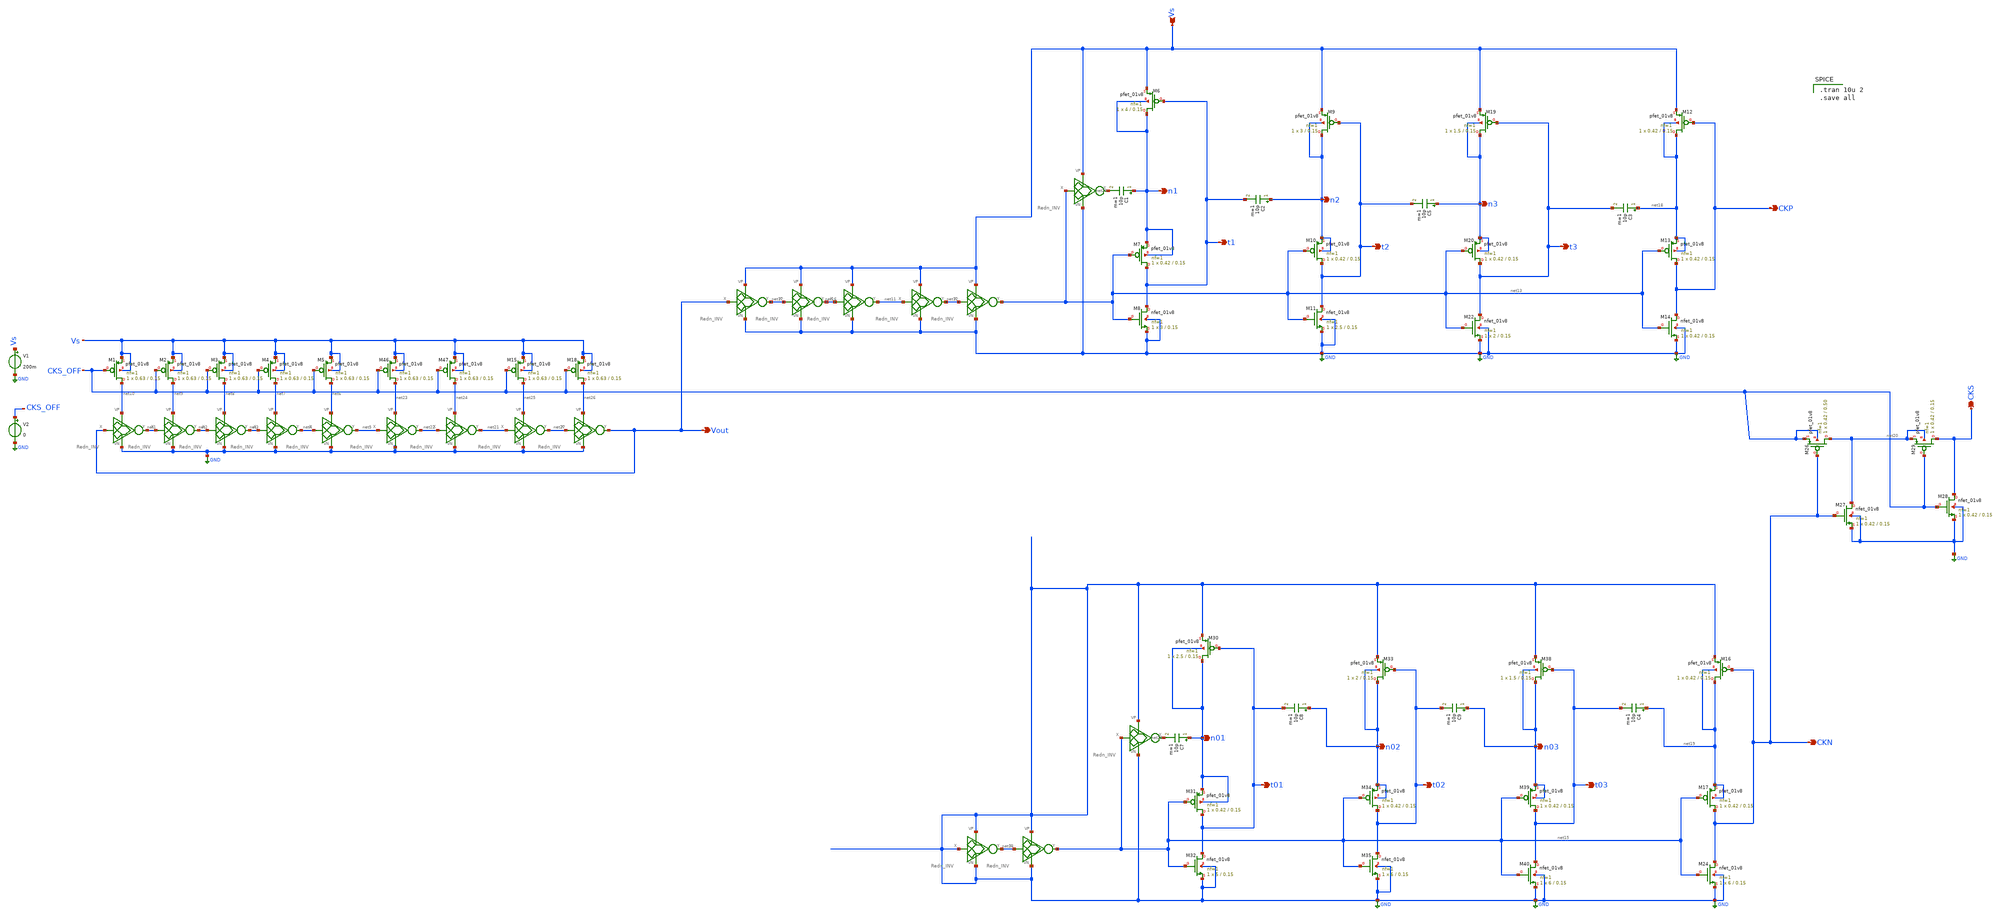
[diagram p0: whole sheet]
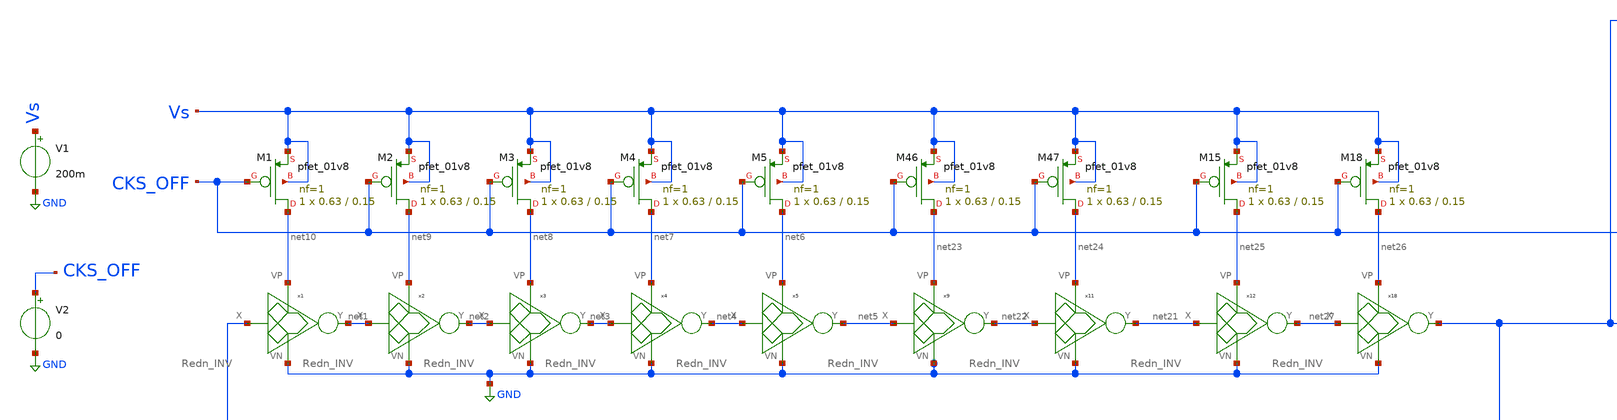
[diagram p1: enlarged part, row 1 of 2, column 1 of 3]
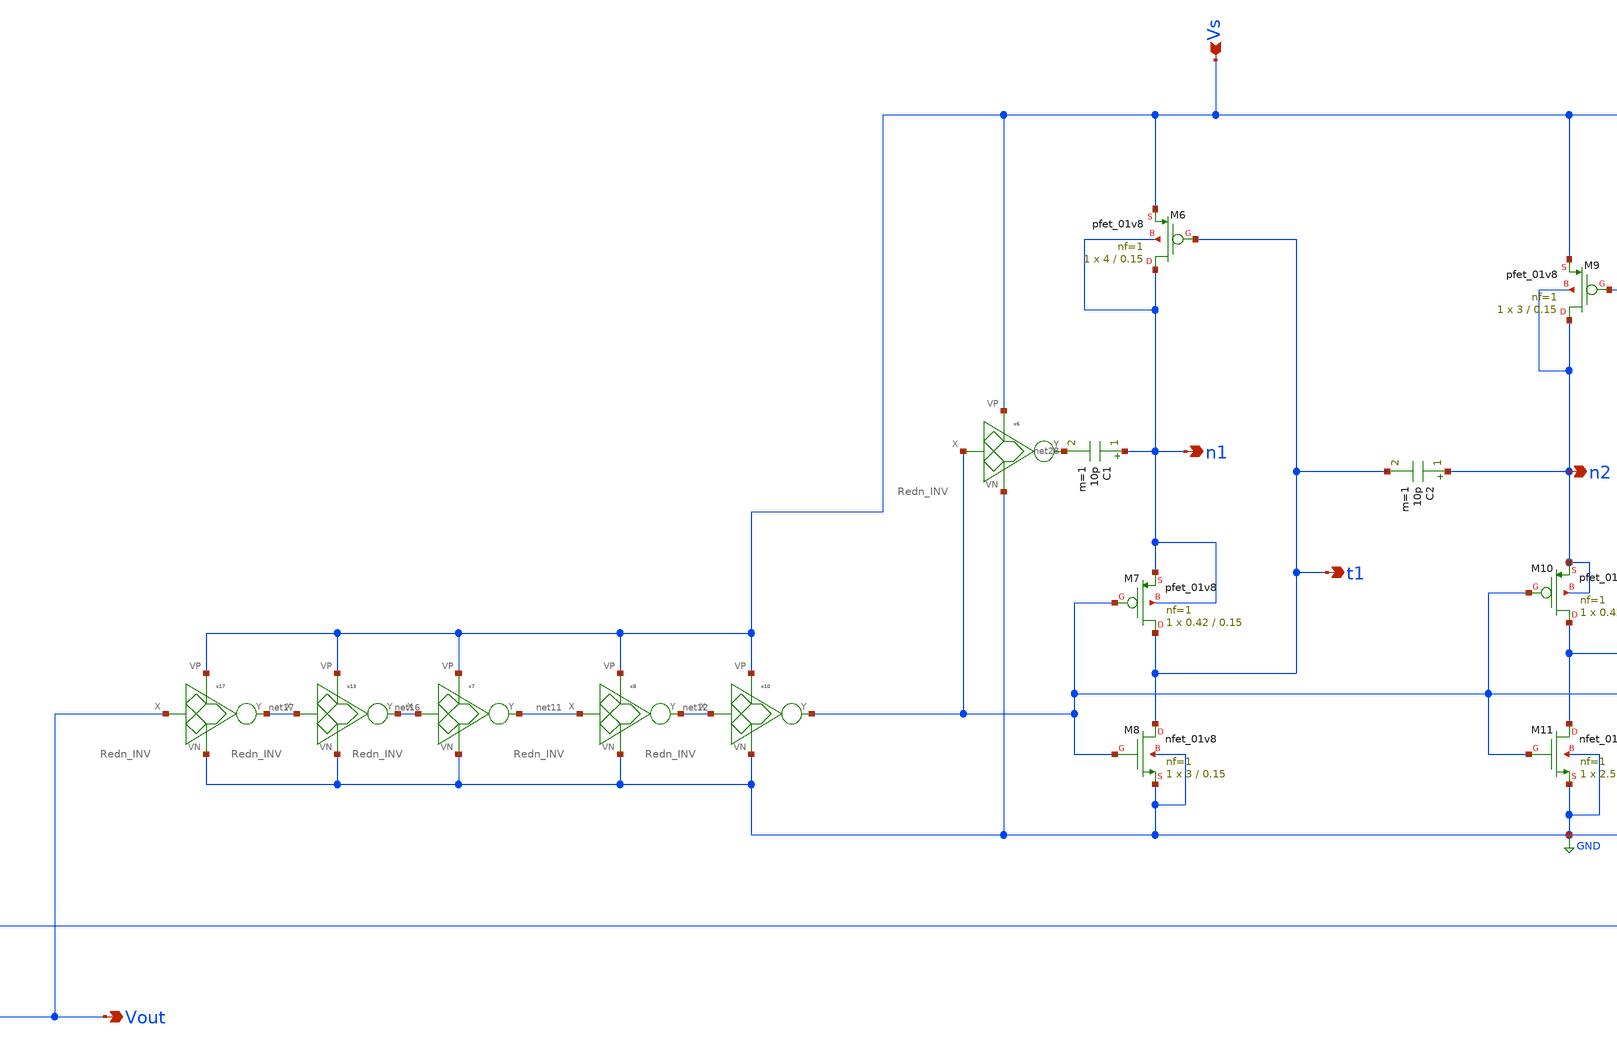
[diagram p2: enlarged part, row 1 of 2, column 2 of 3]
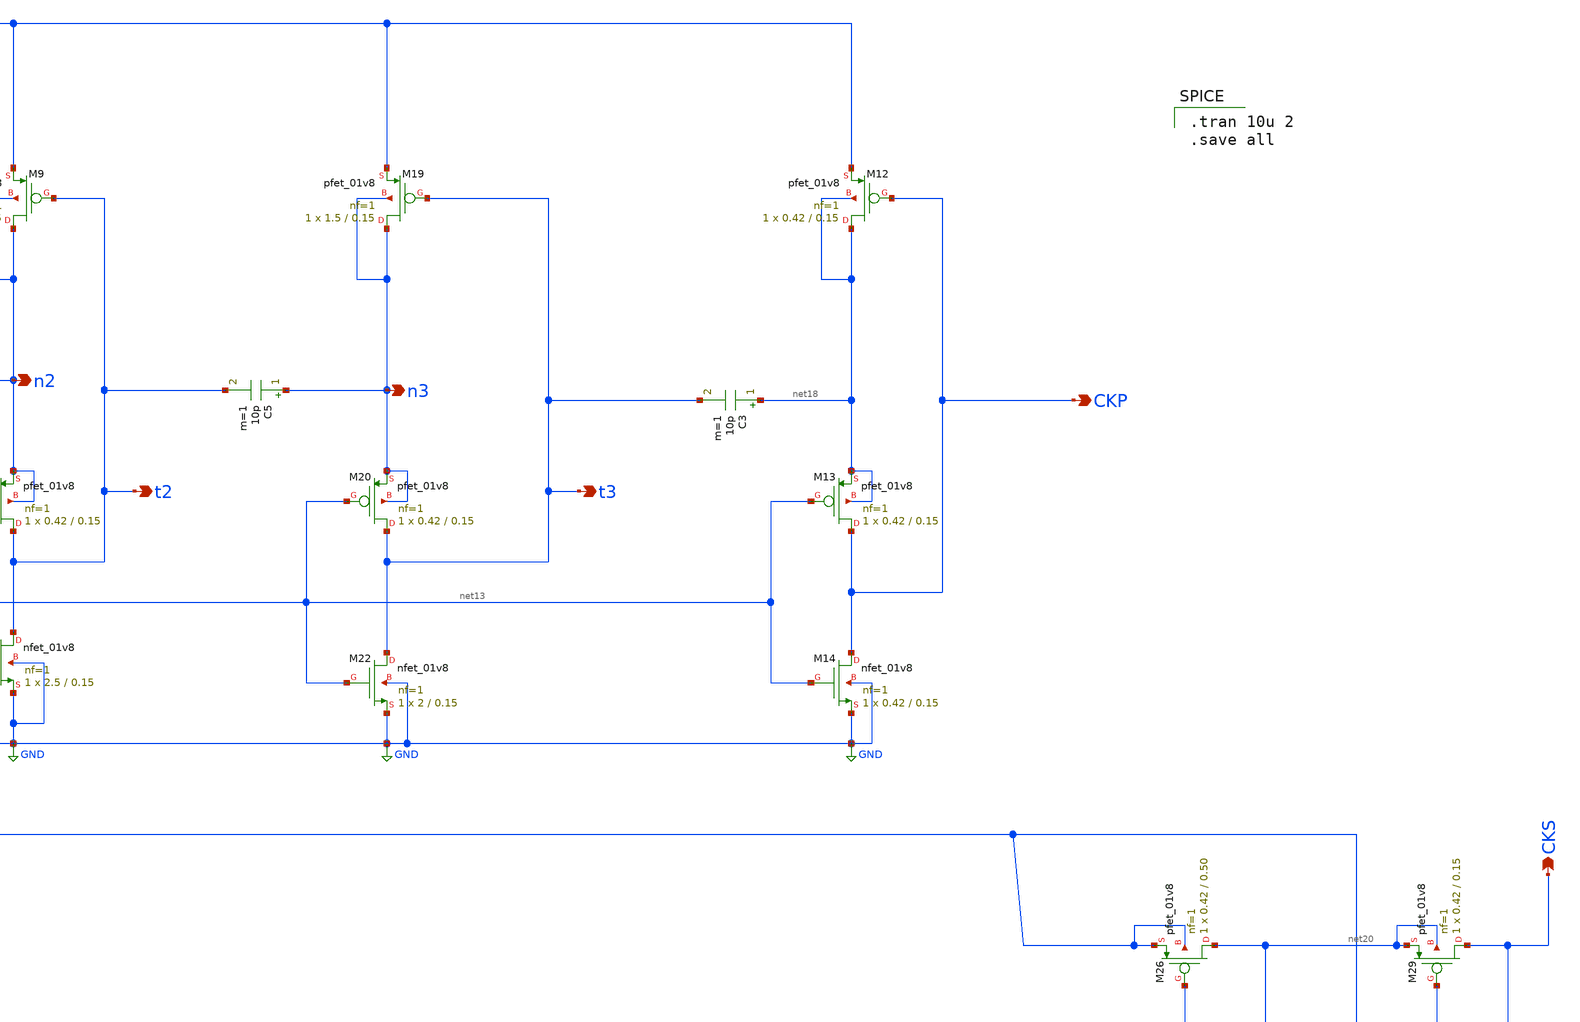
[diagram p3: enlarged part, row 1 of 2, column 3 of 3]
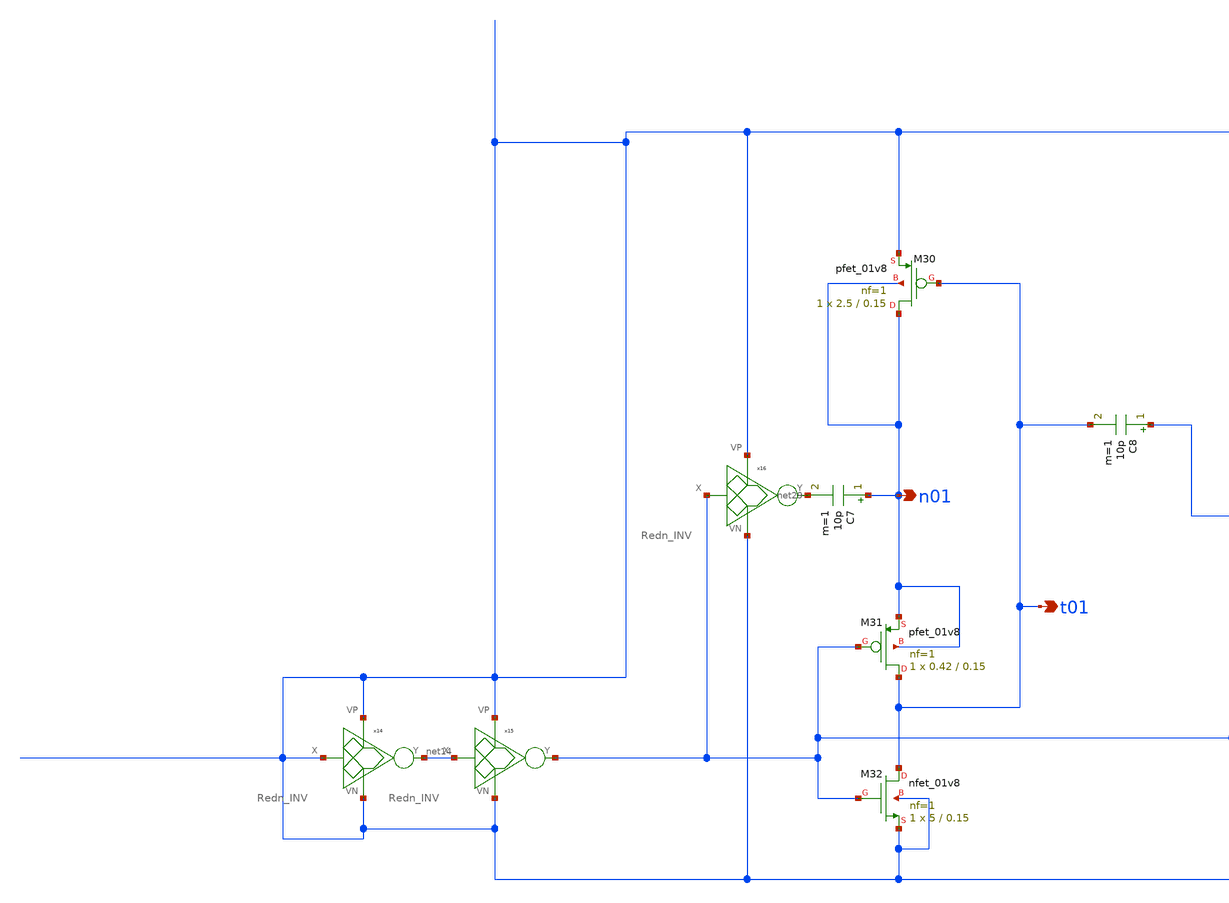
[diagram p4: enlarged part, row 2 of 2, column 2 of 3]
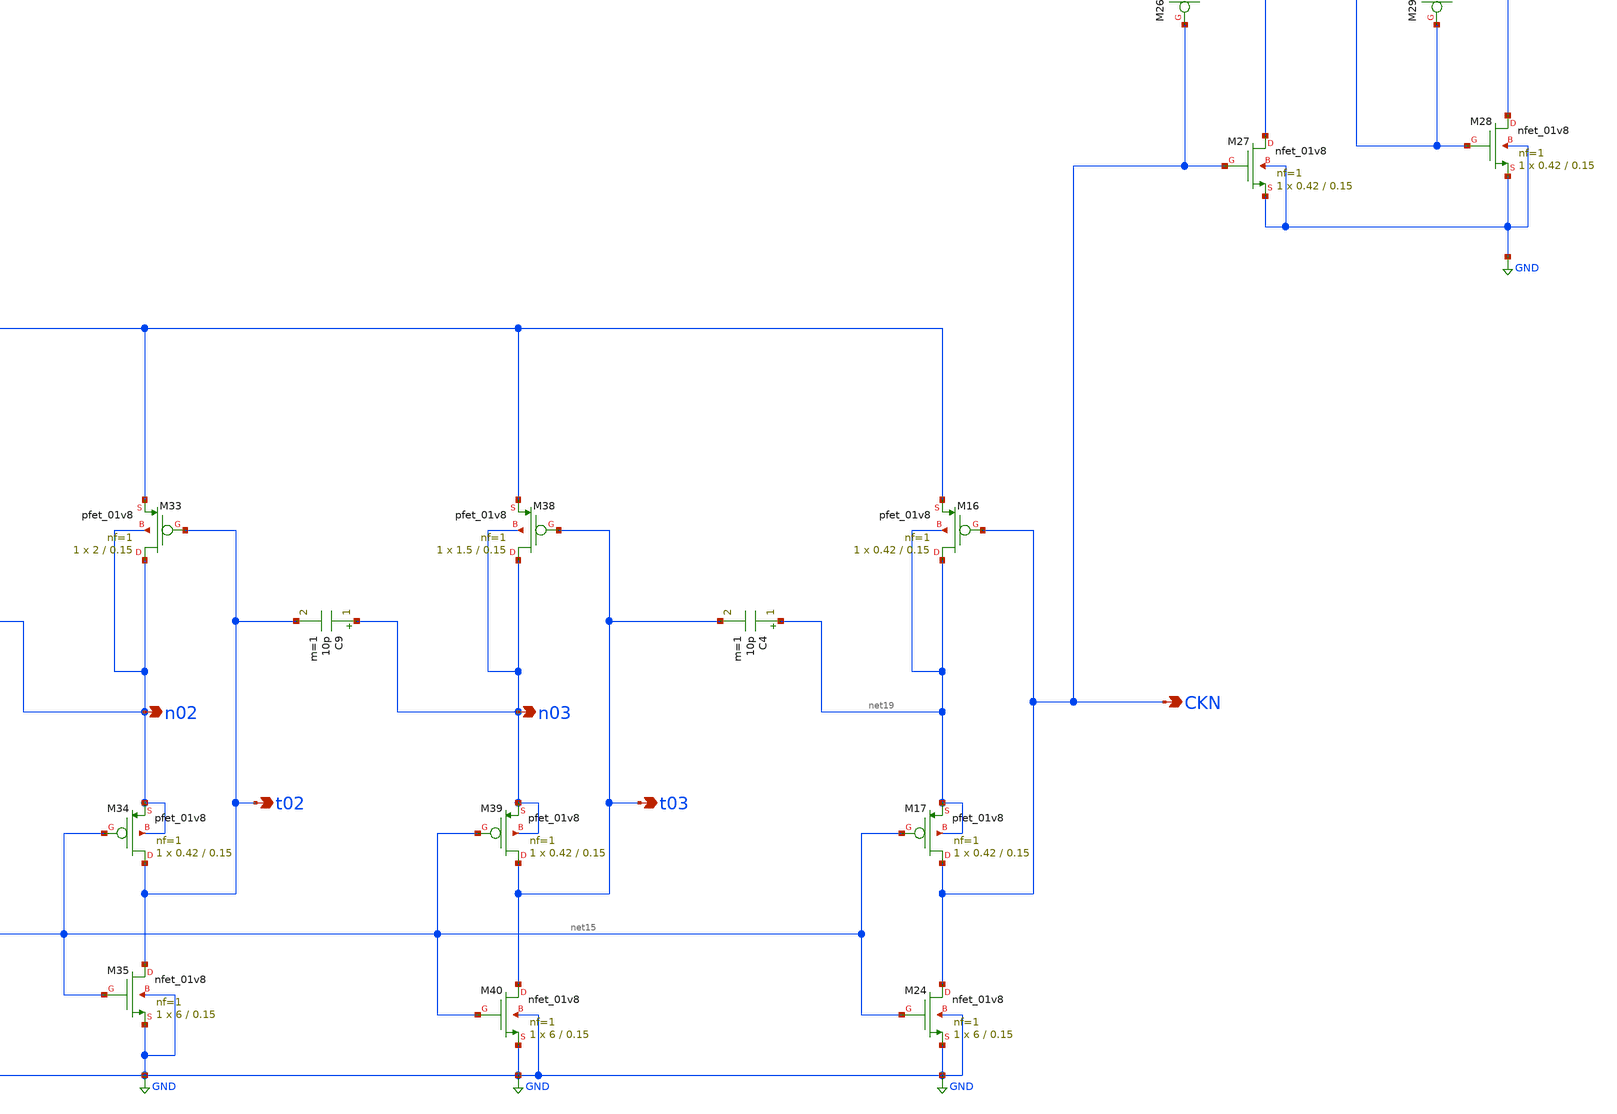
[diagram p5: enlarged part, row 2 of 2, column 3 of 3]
** sch_path: Blocks/Startup Converter/Startup_Conv_4.sch
**.subckt Startup_Conv_4 Vout Vs n1 t2 CKP CKN CKS t3 t1 n2 n3 t01 t02 t03 n01 n02 n03
*.opin Vout
*.ipin Vs
*.opin n1
*.opin t2
*.opin CKP
*.opin CKN
*.opin CKS
*.opin t3
*.opin t1
*.opin n2
*.opin n3
*.opin t01
*.opin t02
*.opin t03
*.opin n01
*.opin n02
*.opin n03
V1 Vs GND 200m
XM1 net10 CKS_OFF Vs Vs sky130_fd_pr__pfet_01v8 L=0.15 W=0.63 nf=1 ad='int((nf+1)/2) * W/nf * 0.29' as='int((nf+2)/2) * W/nf * 0.29'
+ pd='2*int((nf+1)/2) * (W/nf + 0.29)' ps='2*int((nf+2)/2) * (W/nf + 0.29)' nrd='0.29 / W' nrs='0.29 / W'
+ sa=0 sb=0 sd=0 mult=1 m=1
XM2 net9 CKS_OFF Vs Vs sky130_fd_pr__pfet_01v8 L=0.15 W=0.63 nf=1 ad='int((nf+1)/2) * W/nf * 0.29' as='int((nf+2)/2) * W/nf * 0.29'
+ pd='2*int((nf+1)/2) * (W/nf + 0.29)' ps='2*int((nf+2)/2) * (W/nf + 0.29)' nrd='0.29 / W' nrs='0.29 / W'
+ sa=0 sb=0 sd=0 mult=1 m=1
XM3 net8 CKS_OFF Vs Vs sky130_fd_pr__pfet_01v8 L=0.15 W=0.63 nf=1 ad='int((nf+1)/2) * W/nf * 0.29' as='int((nf+2)/2) * W/nf * 0.29'
+ pd='2*int((nf+1)/2) * (W/nf + 0.29)' ps='2*int((nf+2)/2) * (W/nf + 0.29)' nrd='0.29 / W' nrs='0.29 / W'
+ sa=0 sb=0 sd=0 mult=1 m=1
XM4 net7 CKS_OFF Vs Vs sky130_fd_pr__pfet_01v8 L=0.15 W=0.63 nf=1 ad='int((nf+1)/2) * W/nf * 0.29' as='int((nf+2)/2) * W/nf * 0.29'
+ pd='2*int((nf+1)/2) * (W/nf + 0.29)' ps='2*int((nf+2)/2) * (W/nf + 0.29)' nrd='0.29 / W' nrs='0.29 / W'
+ sa=0 sb=0 sd=0 mult=1 m=1
XM5 net6 CKS_OFF Vs Vs sky130_fd_pr__pfet_01v8 L=0.15 W=0.63 nf=1 ad='int((nf+1)/2) * W/nf * 0.29' as='int((nf+2)/2) * W/nf * 0.29'
+ pd='2*int((nf+1)/2) * (W/nf + 0.29)' ps='2*int((nf+2)/2) * (W/nf + 0.29)' nrd='0.29 / W' nrs='0.29 / W'
+ sa=0 sb=0 sd=0 mult=1 m=1
V2 CKS_OFF GND 0
x1 Vout net1 net10 GND Redn_INV
x2 net1 net2 net9 GND Redn_INV
x3 net2 net3 net8 GND Redn_INV
x4 net3 net4 net7 GND Redn_INV
x5 net4 net5 net6 GND Redn_INV
C1 n1 net28 10p m=1
XM6 n1 t1 Vs n1 sky130_fd_pr__pfet_01v8 L=0.15 W=4 nf=1 ad='int((nf+1)/2) * W/nf * 0.29' as='int((nf+2)/2) * W/nf * 0.29'
+ pd='2*int((nf+1)/2) * (W/nf + 0.29)' ps='2*int((nf+2)/2) * (W/nf + 0.29)' nrd='0.29 / W' nrs='0.29 / W'
+ sa=0 sb=0 sd=0 mult=1 m=1
XM7 t1 net13 n1 n1 sky130_fd_pr__pfet_01v8 L=0.15 W=0.42 nf=1 ad='int((nf+1)/2) * W/nf * 0.29' as='int((nf+2)/2) * W/nf * 0.29'
+ pd='2*int((nf+1)/2) * (W/nf + 0.29)' ps='2*int((nf+2)/2) * (W/nf + 0.29)' nrd='0.29 / W' nrs='0.29 / W'
+ sa=0 sb=0 sd=0 mult=1 m=1
XM8 t1 net13 GND GND sky130_fd_pr__nfet_01v8 L=0.15 W=3 nf=1 ad='int((nf+1)/2) * W/nf * 0.29' as='int((nf+2)/2) * W/nf * 0.29'
+ pd='2*int((nf+1)/2) * (W/nf + 0.29)' ps='2*int((nf+2)/2) * (W/nf + 0.29)' nrd='0.29 / W' nrs='0.29 / W'
+ sa=0 sb=0 sd=0 mult=1 m=1
XM9 n2 t2 Vs n2 sky130_fd_pr__pfet_01v8 L=0.15 W=3 nf=1 ad='int((nf+1)/2) * W/nf * 0.29' as='int((nf+2)/2) * W/nf * 0.29'
+ pd='2*int((nf+1)/2) * (W/nf + 0.29)' ps='2*int((nf+2)/2) * (W/nf + 0.29)' nrd='0.29 / W' nrs='0.29 / W'
+ sa=0 sb=0 sd=0 mult=1 m=1
XM10 t2 net13 n2 n2 sky130_fd_pr__pfet_01v8 L=0.15 W=0.42 nf=1 ad='int((nf+1)/2) * W/nf * 0.29' as='int((nf+2)/2) * W/nf * 0.29'
+ pd='2*int((nf+1)/2) * (W/nf + 0.29)' ps='2*int((nf+2)/2) * (W/nf + 0.29)' nrd='0.29 / W' nrs='0.29 / W'
+ sa=0 sb=0 sd=0 mult=1 m=1
XM11 t2 net13 GND GND sky130_fd_pr__nfet_01v8 L=0.15 W=2.5 nf=1 ad='int((nf+1)/2) * W/nf * 0.29' as='int((nf+2)/2) * W/nf * 0.29'
+ pd='2*int((nf+1)/2) * (W/nf + 0.29)' ps='2*int((nf+2)/2) * (W/nf + 0.29)' nrd='0.29 / W' nrs='0.29 / W'
+ sa=0 sb=0 sd=0 mult=1 m=1
C2 n2 t1 10p m=1
x7 net16 net11 Vs GND Redn_INV
x8 net11 net12 Vs GND Redn_INV
x10 net12 net13 Vs GND Redn_INV
x6 net13 net28 Vs GND Redn_INV
XM19 n3 t3 Vs n3 sky130_fd_pr__pfet_01v8 L=0.15 W=1.5 nf=1 ad='int((nf+1)/2) * W/nf * 0.29' as='int((nf+2)/2) * W/nf * 0.29'
+ pd='2*int((nf+1)/2) * (W/nf + 0.29)' ps='2*int((nf+2)/2) * (W/nf + 0.29)' nrd='0.29 / W' nrs='0.29 / W'
+ sa=0 sb=0 sd=0 mult=1 m=1
XM20 t3 net13 n3 n3 sky130_fd_pr__pfet_01v8 L=0.15 W=0.42 nf=1 ad='int((nf+1)/2) * W/nf * 0.29' as='int((nf+2)/2) * W/nf * 0.29'
+ pd='2*int((nf+1)/2) * (W/nf + 0.29)' ps='2*int((nf+2)/2) * (W/nf + 0.29)' nrd='0.29 / W' nrs='0.29 / W'
+ sa=0 sb=0 sd=0 mult=1 m=1
XM22 t3 net13 GND GND sky130_fd_pr__nfet_01v8 L=0.15 W=2 nf=1 ad='int((nf+1)/2) * W/nf * 0.29' as='int((nf+2)/2) * W/nf * 0.29'
+ pd='2*int((nf+1)/2) * (W/nf + 0.29)' ps='2*int((nf+2)/2) * (W/nf + 0.29)' nrd='0.29 / W' nrs='0.29 / W'
+ sa=0 sb=0 sd=0 mult=1 m=1
C5 n3 t2 10p m=1
C7 n01 net29 10p m=1
XM30 n01 t01 GND n01 sky130_fd_pr__pfet_01v8 L=0.15 W=2.5 nf=1 ad='int((nf+1)/2) * W/nf * 0.29' as='int((nf+2)/2) * W/nf * 0.29'
+ pd='2*int((nf+1)/2) * (W/nf + 0.29)' ps='2*int((nf+2)/2) * (W/nf + 0.29)' nrd='0.29 / W' nrs='0.29 / W'
+ sa=0 sb=0 sd=0 mult=1 m=1
XM31 t01 net15 n01 n01 sky130_fd_pr__pfet_01v8 L=0.15 W=0.42 nf=1 ad='int((nf+1)/2) * W/nf * 0.29' as='int((nf+2)/2) * W/nf * 0.29'
+ pd='2*int((nf+1)/2) * (W/nf + 0.29)' ps='2*int((nf+2)/2) * (W/nf + 0.29)' nrd='0.29 / W' nrs='0.29 / W'
+ sa=0 sb=0 sd=0 mult=1 m=1
XM32 t01 net15 GND GND sky130_fd_pr__nfet_01v8 L=0.15 W=5 nf=1 ad='int((nf+1)/2) * W/nf * 0.29' as='int((nf+2)/2) * W/nf * 0.29'
+ pd='2*int((nf+1)/2) * (W/nf + 0.29)' ps='2*int((nf+2)/2) * (W/nf + 0.29)' nrd='0.29 / W' nrs='0.29 / W'
+ sa=0 sb=0 sd=0 mult=1 m=1
XM33 n02 t02 GND n02 sky130_fd_pr__pfet_01v8 L=0.15 W=2 nf=1 ad='int((nf+1)/2) * W/nf * 0.29' as='int((nf+2)/2) * W/nf * 0.29'
+ pd='2*int((nf+1)/2) * (W/nf + 0.29)' ps='2*int((nf+2)/2) * (W/nf + 0.29)' nrd='0.29 / W' nrs='0.29 / W'
+ sa=0 sb=0 sd=0 mult=1 m=1
XM34 t02 net15 n02 n02 sky130_fd_pr__pfet_01v8 L=0.15 W=0.42 nf=1 ad='int((nf+1)/2) * W/nf * 0.29' as='int((nf+2)/2) * W/nf * 0.29'
+ pd='2*int((nf+1)/2) * (W/nf + 0.29)' ps='2*int((nf+2)/2) * (W/nf + 0.29)' nrd='0.29 / W' nrs='0.29 / W'
+ sa=0 sb=0 sd=0 mult=1 m=1
XM35 t02 net15 GND GND sky130_fd_pr__nfet_01v8 L=0.15 W=6 nf=1 ad='int((nf+1)/2) * W/nf * 0.29' as='int((nf+2)/2) * W/nf * 0.29'
+ pd='2*int((nf+1)/2) * (W/nf + 0.29)' ps='2*int((nf+2)/2) * (W/nf + 0.29)' nrd='0.29 / W' nrs='0.29 / W'
+ sa=0 sb=0 sd=0 mult=1 m=1
C8 n02 t01 10p m=1
x14 GND net14 GND GND Redn_INV
x15 net14 net15 GND GND Redn_INV
x16 net15 net29 GND GND Redn_INV
XM38 n03 t03 GND n03 sky130_fd_pr__pfet_01v8 L=0.15 W=1.5 nf=1 ad='int((nf+1)/2) * W/nf * 0.29' as='int((nf+2)/2) * W/nf * 0.29'
+ pd='2*int((nf+1)/2) * (W/nf + 0.29)' ps='2*int((nf+2)/2) * (W/nf + 0.29)' nrd='0.29 / W' nrs='0.29 / W'
+ sa=0 sb=0 sd=0 mult=1 m=1
XM39 t03 net15 n03 n03 sky130_fd_pr__pfet_01v8 L=0.15 W=0.42 nf=1 ad='int((nf+1)/2) * W/nf * 0.29' as='int((nf+2)/2) * W/nf * 0.29'
+ pd='2*int((nf+1)/2) * (W/nf + 0.29)' ps='2*int((nf+2)/2) * (W/nf + 0.29)' nrd='0.29 / W' nrs='0.29 / W'
+ sa=0 sb=0 sd=0 mult=1 m=1
XM40 t03 net15 GND GND sky130_fd_pr__nfet_01v8 L=0.15 W=6 nf=1 ad='int((nf+1)/2) * W/nf * 0.29' as='int((nf+2)/2) * W/nf * 0.29'
+ pd='2*int((nf+1)/2) * (W/nf + 0.29)' ps='2*int((nf+2)/2) * (W/nf + 0.29)' nrd='0.29 / W' nrs='0.29 / W'
+ sa=0 sb=0 sd=0 mult=1 m=1
C9 n03 t02 10p m=1
x13 net17 net16 Vs GND Redn_INV
x17 Vout net17 Vs GND Redn_INV
XM12 net18 CKP Vs net18 sky130_fd_pr__pfet_01v8 L=0.15 W=0.42 nf=1 ad='int((nf+1)/2) * W/nf * 0.29' as='int((nf+2)/2) * W/nf * 0.29'
+ pd='2*int((nf+1)/2) * (W/nf + 0.29)' ps='2*int((nf+2)/2) * (W/nf + 0.29)' nrd='0.29 / W' nrs='0.29 / W'
+ sa=0 sb=0 sd=0 mult=1 m=1
XM13 CKP net13 net18 net18 sky130_fd_pr__pfet_01v8 L=0.15 W=0.42 nf=1 ad='int((nf+1)/2) * W/nf * 0.29'
+ as='int((nf+2)/2) * W/nf * 0.29' pd='2*int((nf+1)/2) * (W/nf + 0.29)' ps='2*int((nf+2)/2) * (W/nf + 0.29)'
+ nrd='0.29 / W' nrs='0.29 / W' sa=0 sb=0 sd=0 mult=1 m=1
XM14 CKP net13 GND GND sky130_fd_pr__nfet_01v8 L=0.15 W=0.42 nf=1 ad='int((nf+1)/2) * W/nf * 0.29' as='int((nf+2)/2) * W/nf * 0.29'
+ pd='2*int((nf+1)/2) * (W/nf + 0.29)' ps='2*int((nf+2)/2) * (W/nf + 0.29)' nrd='0.29 / W' nrs='0.29 / W'
+ sa=0 sb=0 sd=0 mult=1 m=1
C3 net18 t3 10p m=1
XM16 net19 CKN GND net19 sky130_fd_pr__pfet_01v8 L=0.15 W=0.42 nf=1 ad='int((nf+1)/2) * W/nf * 0.29'
+ as='int((nf+2)/2) * W/nf * 0.29' pd='2*int((nf+1)/2) * (W/nf + 0.29)' ps='2*int((nf+2)/2) * (W/nf + 0.29)'
+ nrd='0.29 / W' nrs='0.29 / W' sa=0 sb=0 sd=0 mult=1 m=1
XM17 CKN net15 net19 net19 sky130_fd_pr__pfet_01v8 L=0.15 W=0.42 nf=1 ad='int((nf+1)/2) * W/nf * 0.29'
+ as='int((nf+2)/2) * W/nf * 0.29' pd='2*int((nf+1)/2) * (W/nf + 0.29)' ps='2*int((nf+2)/2) * (W/nf + 0.29)'
+ nrd='0.29 / W' nrs='0.29 / W' sa=0 sb=0 sd=0 mult=1 m=1
XM24 CKN net15 GND GND sky130_fd_pr__nfet_01v8 L=0.15 W=6 nf=1 ad='int((nf+1)/2) * W/nf * 0.29' as='int((nf+2)/2) * W/nf * 0.29'
+ pd='2*int((nf+1)/2) * (W/nf + 0.29)' ps='2*int((nf+2)/2) * (W/nf + 0.29)' nrd='0.29 / W' nrs='0.29 / W'
+ sa=0 sb=0 sd=0 mult=1 m=1
C4 net19 t03 10p m=1
XM26 net20 CKN CKS_OFF CKS_OFF sky130_fd_pr__pfet_01v8 L=0.50 W=0.42 nf=1 ad='int((nf+1)/2) * W/nf * 0.29'
+ as='int((nf+2)/2) * W/nf * 0.29' pd='2*int((nf+1)/2) * (W/nf + 0.29)' ps='2*int((nf+2)/2) * (W/nf + 0.29)'
+ nrd='0.29 / W' nrs='0.29 / W' sa=0 sb=0 sd=0 mult=1 m=1
XM27 net20 CKN GND GND sky130_fd_pr__nfet_01v8 L=0.15 W=0.42 nf=1 ad='int((nf+1)/2) * W/nf * 0.29' as='int((nf+2)/2) * W/nf * 0.29'
+ pd='2*int((nf+1)/2) * (W/nf + 0.29)' ps='2*int((nf+2)/2) * (W/nf + 0.29)' nrd='0.29 / W' nrs='0.29 / W'
+ sa=0 sb=0 sd=0 mult=1 m=1
XM28 CKS CKS_OFF GND GND sky130_fd_pr__nfet_01v8 L=0.15 W=0.42 nf=1 ad='int((nf+1)/2) * W/nf * 0.29'
+ as='int((nf+2)/2) * W/nf * 0.29' pd='2*int((nf+1)/2) * (W/nf + 0.29)' ps='2*int((nf+2)/2) * (W/nf + 0.29)'
+ nrd='0.29 / W' nrs='0.29 / W' sa=0 sb=0 sd=0 mult=1 m=1
XM29 CKS CKS_OFF net20 net20 sky130_fd_pr__pfet_01v8 L=0.15 W=0.42 nf=1 ad='int((nf+1)/2) * W/nf * 0.29'
+ as='int((nf+2)/2) * W/nf * 0.29' pd='2*int((nf+1)/2) * (W/nf + 0.29)' ps='2*int((nf+2)/2) * (W/nf + 0.29)'
+ nrd='0.29 / W' nrs='0.29 / W' sa=0 sb=0 sd=0 mult=1 m=1
x9 net5 net22 net23 GND Redn_INV
x11 net22 net21 net24 GND Redn_INV
XM46 net23 CKS_OFF Vs Vs sky130_fd_pr__pfet_01v8 L=0.15 W=0.63 nf=1 ad='int((nf+1)/2) * W/nf * 0.29'
+ as='int((nf+2)/2) * W/nf * 0.29' pd='2*int((nf+1)/2) * (W/nf + 0.29)' ps='2*int((nf+2)/2) * (W/nf + 0.29)'
+ nrd='0.29 / W' nrs='0.29 / W' sa=0 sb=0 sd=0 mult=1 m=1
XM47 net24 CKS_OFF Vs Vs sky130_fd_pr__pfet_01v8 L=0.15 W=0.63 nf=1 ad='int((nf+1)/2) * W/nf * 0.29'
+ as='int((nf+2)/2) * W/nf * 0.29' pd='2*int((nf+1)/2) * (W/nf + 0.29)' ps='2*int((nf+2)/2) * (W/nf + 0.29)'
+ nrd='0.29 / W' nrs='0.29 / W' sa=0 sb=0 sd=0 mult=1 m=1
x12 net21 net27 net25 GND Redn_INV
XM15 net25 CKS_OFF Vs Vs sky130_fd_pr__pfet_01v8 L=0.15 W=0.63 nf=1 ad='int((nf+1)/2) * W/nf * 0.29'
+ as='int((nf+2)/2) * W/nf * 0.29' pd='2*int((nf+1)/2) * (W/nf + 0.29)' ps='2*int((nf+2)/2) * (W/nf + 0.29)'
+ nrd='0.29 / W' nrs='0.29 / W' sa=0 sb=0 sd=0 mult=1 m=1
x18 net27 Vout net26 GND Redn_INV
XM18 net26 CKS_OFF Vs Vs sky130_fd_pr__pfet_01v8 L=0.15 W=0.63 nf=1 ad='int((nf+1)/2) * W/nf * 0.29'
+ as='int((nf+2)/2) * W/nf * 0.29' pd='2*int((nf+1)/2) * (W/nf + 0.29)' ps='2*int((nf+2)/2) * (W/nf + 0.29)'
+ nrd='0.29 / W' nrs='0.29 / W' sa=0 sb=0 sd=0 mult=1 m=1
**** begin user architecture code

** opencircuitdesign pdks install
.lib $::SKYWATER_MODELS/sky130.lib.spice tt



.tran 10u 2
.save all

**** end user architecture code
**.ends

* expanding   symbol:  component/Reduntant_Inverter/Redn_INV.sym # of pins=4
** sym_path: component/Reduntant_Inverter/Redn_INV.sym
** sch_path: component/Reduntant_Inverter/Redn_INV.sch
.subckt Redn_INV X Y VP VN
*.opin Y
*.ipin X
*.iopin VP
*.iopin VN
XM15 net4 X VN VN sky130_fd_pr__nfet_01v8_lvt L=0.15 W=1 nf=1 ad='int((nf+1)/2) * W/nf * 0.29' as='int((nf+2)/2) * W/nf * 0.29'
+ pd='2*int((nf+1)/2) * (W/nf + 0.29)' ps='2*int((nf+2)/2) * (W/nf + 0.29)' nrd='0.29 / W' nrs='0.29 / W'
+ sa=0 sb=0 sd=0 mult=1 m=1
XM1 net5 X net3 VN sky130_fd_pr__nfet_01v8_lvt L=0.15 W=3.25 nf=1 ad='int((nf+1)/2) * W/nf * 0.29' as='int((nf+2)/2) * W/nf * 0.29'
+ pd='2*int((nf+1)/2) * (W/nf + 0.29)' ps='2*int((nf+2)/2) * (W/nf + 0.29)' nrd='0.29 / W' nrs='0.29 / W'
+ sa=0 sb=0 sd=0 mult=1 m=1
XM16 Y X net6 VN sky130_fd_pr__nfet_01v8_lvt L=0.15 W=6.5 nf=1 ad='int((nf+1)/2) * W/nf * 0.29' as='int((nf+2)/2) * W/nf * 0.29'
+ pd='2*int((nf+1)/2) * (W/nf + 0.29)' ps='2*int((nf+2)/2) * (W/nf + 0.29)' nrd='0.29 / W' nrs='0.29 / W'
+ sa=0 sb=0 sd=0 mult=1 m=1
XM17 net3 X VN VN sky130_fd_pr__nfet_01v8_lvt L=0.15 W=3.25 nf=1 ad='int((nf+1)/2) * W/nf * 0.29' as='int((nf+2)/2) * W/nf * 0.29'
+ pd='2*int((nf+1)/2) * (W/nf + 0.29)' ps='2*int((nf+2)/2) * (W/nf + 0.29)' nrd='0.29 / W' nrs='0.29 / W'
+ sa=0 sb=0 sd=0 mult=1 m=1
XM18 net2 X VN VN sky130_fd_pr__nfet_01v8_lvt L=0.15 W=1.5 nf=1 ad='int((nf+1)/2) * W/nf * 0.29' as='int((nf+2)/2) * W/nf * 0.29'
+ pd='2*int((nf+1)/2) * (W/nf + 0.29)' ps='2*int((nf+2)/2) * (W/nf + 0.29)' nrd='0.29 / W' nrs='0.29 / W'
+ sa=0 sb=0 sd=0 mult=1 m=1
XM19 net1 X VN VN sky130_fd_pr__nfet_01v8_lvt L=0.15 W=6.5 nf=1 ad='int((nf+1)/2) * W/nf * 0.29' as='int((nf+2)/2) * W/nf * 0.29'
+ pd='2*int((nf+1)/2) * (W/nf + 0.29)' ps='2*int((nf+2)/2) * (W/nf + 0.29)' nrd='0.29 / W' nrs='0.29 / W'
+ sa=0 sb=0 sd=0 mult=1 m=1
XM20 net6 X net1 VN sky130_fd_pr__nfet_01v8_lvt L=0.15 W=6.5 nf=1 ad='int((nf+1)/2) * W/nf * 0.29' as='int((nf+2)/2) * W/nf * 0.29'
+ pd='2*int((nf+1)/2) * (W/nf + 0.29)' ps='2*int((nf+2)/2) * (W/nf + 0.29)' nrd='0.29 / W' nrs='0.29 / W'
+ sa=0 sb=0 sd=0 mult=1 m=1
XM2 net4 X VP VP sky130_fd_pr__pfet_01v8 L=0.15 W=10 nf=1 ad='int((nf+1)/2) * W/nf * 0.29' as='int((nf+2)/2) * W/nf * 0.29'
+ pd='2*int((nf+1)/2) * (W/nf + 0.29)' ps='2*int((nf+2)/2) * (W/nf + 0.29)' nrd='0.29 / W' nrs='0.29 / W'
+ sa=0 sb=0 sd=0 mult=1 m=1
XM5 net5 X net4 net4 sky130_fd_pr__pfet_01v8 L=0.15 W=10 nf=1 ad='int((nf+1)/2) * W/nf * 0.29' as='int((nf+2)/2) * W/nf * 0.29'
+ pd='2*int((nf+1)/2) * (W/nf + 0.29)' ps='2*int((nf+2)/2) * (W/nf + 0.29)' nrd='0.29 / W' nrs='0.29 / W'
+ sa=0 sb=0 sd=0 mult=1 m=1
XM6 Y X net5 VP sky130_fd_pr__pfet_01v8 L=0.15 W=10 nf=1 ad='int((nf+1)/2) * W/nf * 0.29' as='int((nf+2)/2) * W/nf * 0.29'
+ pd='2*int((nf+1)/2) * (W/nf + 0.29)' ps='2*int((nf+2)/2) * (W/nf + 0.29)' nrd='0.29 / W' nrs='0.29 / W'
+ sa=0 sb=0 sd=0 mult=1 m=1
XM8 net3 X VP VP sky130_fd_pr__pfet_01v8 L=0.15 W=2 nf=1 ad='int((nf+1)/2) * W/nf * 0.29' as='int((nf+2)/2) * W/nf * 0.29'
+ pd='2*int((nf+1)/2) * (W/nf + 0.29)' ps='2*int((nf+2)/2) * (W/nf + 0.29)' nrd='0.29 / W' nrs='0.29 / W'
+ sa=0 sb=0 sd=0 mult=1 m=1
XM12 net2 X VP VP sky130_fd_pr__pfet_01v8 L=0.15 W=5 nf=1 ad='int((nf+1)/2) * W/nf * 0.29' as='int((nf+2)/2) * W/nf * 0.29'
+ pd='2*int((nf+1)/2) * (W/nf + 0.29)' ps='2*int((nf+2)/2) * (W/nf + 0.29)' nrd='0.29 / W' nrs='0.29 / W'
+ sa=0 sb=0 sd=0 mult=1 m=1
XM14 net6 X net2 VP sky130_fd_pr__pfet_01v8 L=0.15 W=5 nf=1 ad='int((nf+1)/2) * W/nf * 0.29' as='int((nf+2)/2) * W/nf * 0.29'
+ pd='2*int((nf+1)/2) * (W/nf + 0.29)' ps='2*int((nf+2)/2) * (W/nf + 0.29)' nrd='0.29 / W' nrs='0.29 / W'
+ sa=0 sb=0 sd=0 mult=1 m=1
XM21 net1 X VP VP sky130_fd_pr__pfet_01v8 L=0.15 W=1.5 nf=1 ad='int((nf+1)/2) * W/nf * 0.29' as='int((nf+2)/2) * W/nf * 0.29'
+ pd='2*int((nf+1)/2) * (W/nf + 0.29)' ps='2*int((nf+2)/2) * (W/nf + 0.29)' nrd='0.29 / W' nrs='0.29 / W'
+ sa=0 sb=0 sd=0 mult=1 m=1
.ends

.GLOBAL GND
.end
